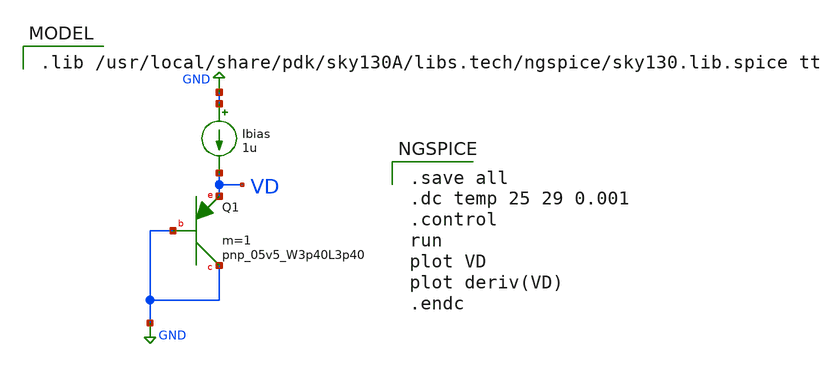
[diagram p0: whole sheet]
** sch_path: 1_diode_3p4_VD_temp.sch
**.subckt 1_diode_3p4_VD_temp
Ibias GND VD 1u
XQ1 GND GND VD sky130_fd_pr__pnp_05v5_W3p40L3p40 m=1
**** begin user architecture code

.save all
.dc temp 25 29 0.001
.control
run
plot VD
plot deriv(VD)
.endc


.lib /usr/local/share/pdk/sky130A/libs.tech/ngspice/sky130.lib.spice tt

**** end user architecture code
**.ends
.GLOBAL GND
.end
